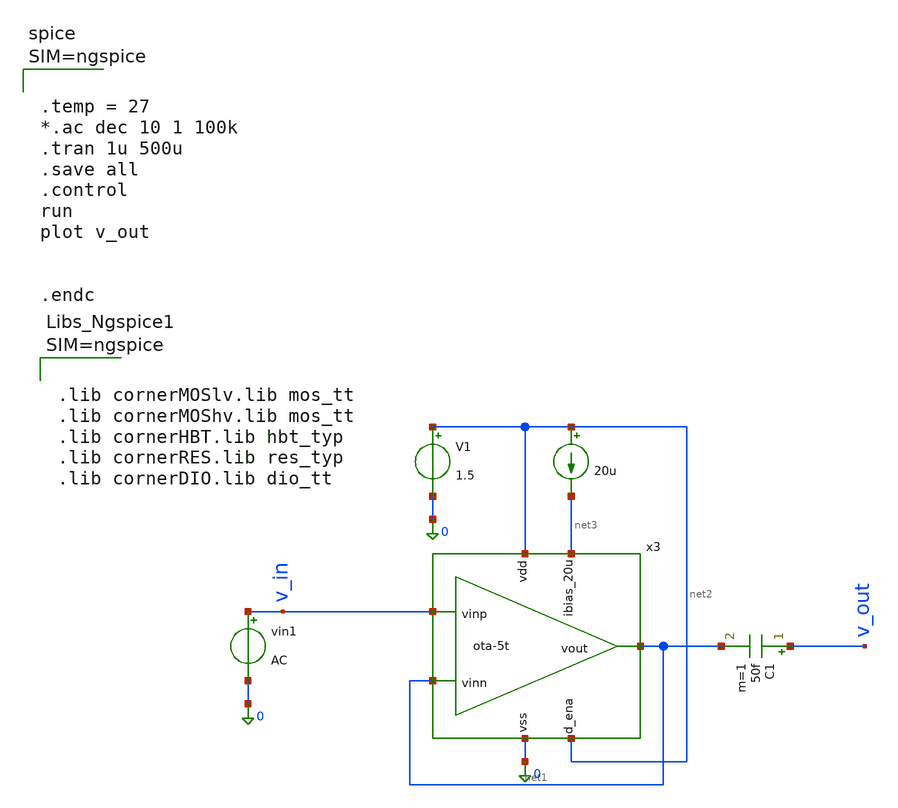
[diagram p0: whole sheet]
** sch_path: 004_Real_Circuits/5T_ota_tb.sch
* 004_Real_Circuits/ota-5t.sch:
* (c) 2024-2025 Harald Pretl, Apache-2.0 license
**.subckt 5T_ota_tb
V1 net2 0 1.5
I0 net2 net3 20u
vin1 v_in 0 AC
C1 v_out net1 50f m=1
x3 net2 net1 v_in net1 net3 net2 0 ota-5t
**** begin user architecture code



.lib cornerMOSlv.lib mos_tt
.lib cornerMOShv.lib mos_tt
.lib cornerHBT.lib hbt_typ
.lib cornerRES.lib res_typ
.lib cornerDIO.lib dio_tt






.temp = 27
*.ac dec 10 1 100k
.tran 1u 500u
.save all
.control
run
plot v_out


.endc



**** end user architecture code
**.ends

* expanding   symbol:  /foss/designs/GitHub_Repo/004_Real_Circuits/ota-5t.sym # of pins=7
** sym_path: /foss/designs/GitHub_Repo/004_Real_Circuits/ota-5t.sym
** sch_path: /foss/designs/GitHub_Repo/004_Real_Circuits/ota-5t.sch
.subckt ota-5t vdd vout vinp vinn ibias_20u d_ena vss
*.ipin ibias_20u
*.iopin vdd
*.iopin vss
*.ipin vinp
*.ipin vinn
*.opin vout
*.ipin d_ena
XM5 tail gate_n vss vss sg13_lv_nmos w=1.0u l=5u ng=1 m=1 mm_ok=1
XM4 vout gate_p vdd vdd sg13_lv_pmos w=2.5u l=5u ng=1 m=1 mm_ok=1
XM1 gate_p vinp tail vss sg13_lv_nmos w=2u l=5u ng=1 m=1 mm_ok=1
XM2 vout vinn tail vss sg13_lv_nmos w=2u l=5u ng=1 m=1 mm_ok=1
XM3 gate_p gate_p vdd vdd sg13_lv_pmos w=2.5u l=5u ng=1 m=1 mm_ok=1
XM6 ibias_20u gate_n vss vss sg13_lv_nmos w=6.5u l=5u ng=5 m=1 mm_ok=1
XM9 gate_n ena_n vss vss sg13_lv_nmos w=0.5u l=0.13u ng=1 m=1 mm_ok=1
XM11 gate_p ena vdd vdd sg13_lv_pmos w=1.5u l=0.13u ng=1 m=1 mm_ok=1
XM7 ena ena_n vss vss sg13_lv_nmos w=0.5u l=0.13u ng=1 m=1 mm_ok=1
XM8 ena ena_n vdd vdd sg13_lv_pmos w=1.5u l=0.13u ng=1 m=1 mm_ok=1
XM10 ibias_20u ena gate_n vss sg13_lv_nmos w=0.5u l=0.13u ng=1 m=1 mm_ok=1
XM12 ena_n d_ena vss vss sg13_lv_nmos w=0.5u l=0.13u ng=1 m=1 mm_ok=1
XM13 ena_n d_ena vdd vdd sg13_lv_pmos w=1.5u l=0.13u ng=1 m=1 mm_ok=1
.ends

.end
